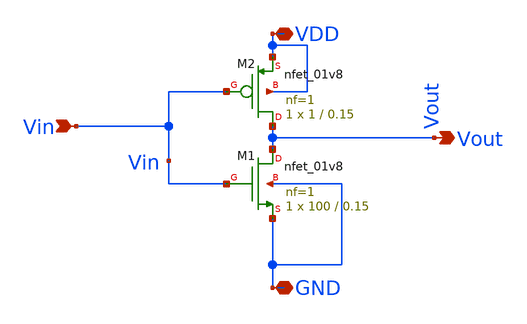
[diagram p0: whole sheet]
** sch_path: pll/xctl_lib_V2/xctl/xschem/Inv.sch
**.subckt Inv Vout Vin VDD GND
*.opin Vout
*.ipin Vin
*.iopin VDD
*.iopin GND
XM1 Vout Vin GND GND sky130_fd_pr__nfet_01v8 L=0.15 W=100 nf=1 ad='int((nf+1)/2) * W/nf * 0.29' as='int((nf+2)/2) * W/nf * 0.29'
+ pd='2*int((nf+1)/2) * (W/nf + 0.29)' ps='2*int((nf+2)/2) * (W/nf + 0.29)' nrd='0.29 / W' nrs='0.29 / W'
+ sa=0 sb=0 sd=0 mult=1 m=1
XM2 Vout Vin VDD VDD sky130_fd_pr__nfet_01v8 L=0.15 W=1 nf=1 ad='int((nf+1)/2) * W/nf * 0.29' as='int((nf+2)/2) * W/nf * 0.29'
+ pd='2*int((nf+1)/2) * (W/nf + 0.29)' ps='2*int((nf+2)/2) * (W/nf + 0.29)' nrd='0.29 / W' nrs='0.29 / W'
+ sa=0 sb=0 sd=0 mult=1 m=1
**.ends
.end
